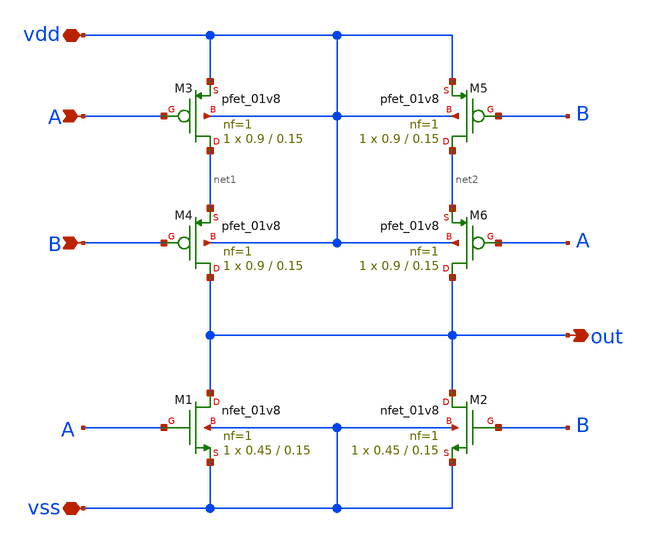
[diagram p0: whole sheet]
** sch_path: xschem/nor.sch
**.subckt nor A B vdd out vss
*.ipin A
*.ipin B
*.iopin vdd
*.opin out
*.iopin vss
XM1 out A vss vss sky130_fd_pr__nfet_01v8 L=0.15 W=0.45 nf=1 ad='int((nf+1)/2) * W/nf * 0.29' as='int((nf+2)/2) * W/nf * 0.29'
+ pd='2*int((nf+1)/2) * (W/nf + 0.29)' ps='2*int((nf+2)/2) * (W/nf + 0.29)' nrd='0.29 / W' nrs='0.29 / W'
+ sa=0 sb=0 sd=0 mult=1 m=1
XM2 out B vss vss sky130_fd_pr__nfet_01v8 L=0.15 W=0.45 nf=1 ad='int((nf+1)/2) * W/nf * 0.29' as='int((nf+2)/2) * W/nf * 0.29'
+ pd='2*int((nf+1)/2) * (W/nf + 0.29)' ps='2*int((nf+2)/2) * (W/nf + 0.29)' nrd='0.29 / W' nrs='0.29 / W'
+ sa=0 sb=0 sd=0 mult=1 m=1
XM4 out B net1 vdd sky130_fd_pr__pfet_01v8 L=0.15 W=0.9 nf=1 ad='int((nf+1)/2) * W/nf * 0.29' as='int((nf+2)/2) * W/nf * 0.29'
+ pd='2*int((nf+1)/2) * (W/nf + 0.29)' ps='2*int((nf+2)/2) * (W/nf + 0.29)' nrd='0.29 / W' nrs='0.29 / W'
+ sa=0 sb=0 sd=0 mult=1 m=1
XM3 net1 A vdd vdd sky130_fd_pr__pfet_01v8 L=0.15 W=0.9 nf=1 ad='int((nf+1)/2) * W/nf * 0.29' as='int((nf+2)/2) * W/nf * 0.29'
+ pd='2*int((nf+1)/2) * (W/nf + 0.29)' ps='2*int((nf+2)/2) * (W/nf + 0.29)' nrd='0.29 / W' nrs='0.29 / W'
+ sa=0 sb=0 sd=0 mult=1 m=1
XM5 net2 B vdd vdd sky130_fd_pr__pfet_01v8 L=0.15 W=0.9 nf=1 ad='int((nf+1)/2) * W/nf * 0.29' as='int((nf+2)/2) * W/nf * 0.29'
+ pd='2*int((nf+1)/2) * (W/nf + 0.29)' ps='2*int((nf+2)/2) * (W/nf + 0.29)' nrd='0.29 / W' nrs='0.29 / W'
+ sa=0 sb=0 sd=0 mult=1 m=1
XM6 out A net2 vdd sky130_fd_pr__pfet_01v8 L=0.15 W=0.9 nf=1 ad='int((nf+1)/2) * W/nf * 0.29' as='int((nf+2)/2) * W/nf * 0.29'
+ pd='2*int((nf+1)/2) * (W/nf + 0.29)' ps='2*int((nf+2)/2) * (W/nf + 0.29)' nrd='0.29 / W' nrs='0.29 / W'
+ sa=0 sb=0 sd=0 mult=1 m=1
**.ends
.end
